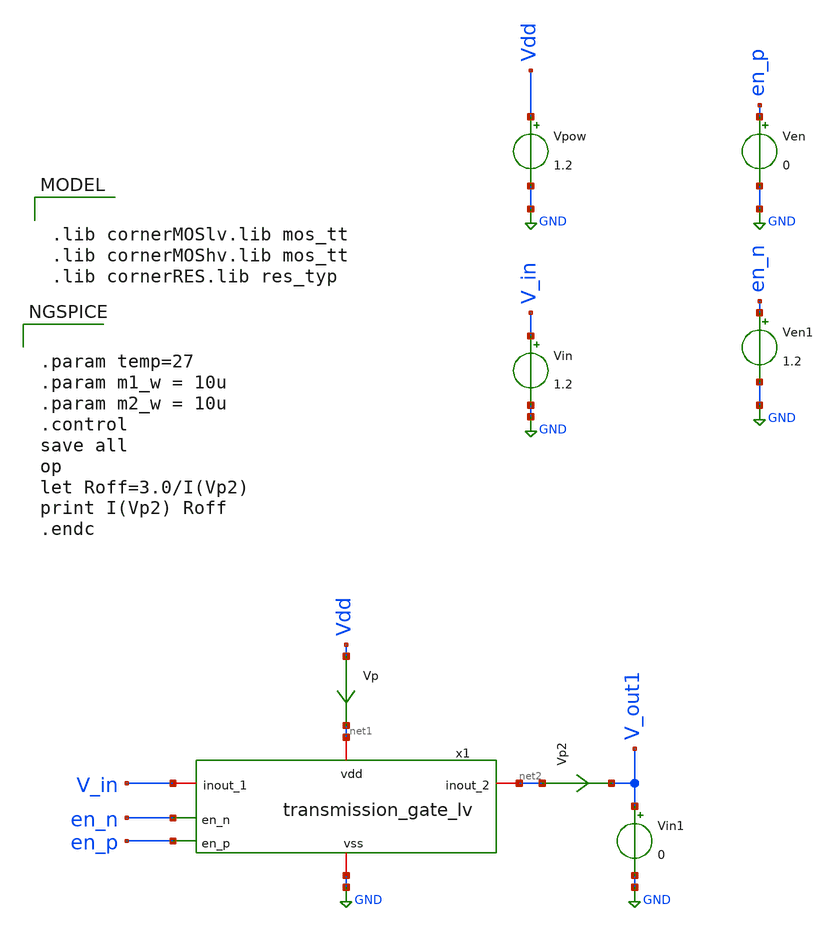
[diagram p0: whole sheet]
** sch_path: design_data/xschem/transmission_gate__lv_tb_Ileak.sch
* Copyright 2023 IHP PDK Authors
**.subckt transmission_gate__lv_tb_Ileak
Vpow Vdd GND 1.2
Vp Vdd net1 0
.save i(vp)
Vin V_in GND 1.2
Ven en_p GND 0
Ven1 en_n GND 1.2
Vp2 net2 V_out1 0
.save i(vp2)
Vin1 V_out1 GND 0
x1 net1 en_n V_in net2 en_p GND transmission_gate_lv
**** begin user architecture code

.lib cornerMOSlv.lib mos_tt
.lib cornerMOShv.lib mos_tt
.lib cornerRES.lib res_typ



.param temp=27
.param m1_w = 10u
.param m2_w = 10u
.control
save all
op
let Roff=3.0/I(Vp2)
print I(Vp2) Roff
.endc


**** end user architecture code
**.ends

* expanding   symbol:  transmission_gate_lv.sym # of pins=6
** sym_path: design_data/xschem/transmission_gate_lv.sym
** sch_path: design_data/xschem/transmission_gate_lv.sch
.subckt transmission_gate_lv vdd en_n inout_1 inout_2 en_p vss
*.iopin inout_1
*.iopin inout_2
*.ipin en_p
*.iopin vdd
*.iopin vss
*.ipin en_n
XR1 vss net1 ptap1 R=1.903 w=20.78e-6 l=20.78e-6
XR2 vdd net2 ntap1 R=1.903 w=20.78e-6 l=20.78e-6
XM2 inout_2 en_n inout_1 net2 sg13_lv_pmos w={m2_w} l=0.13u ng=10 m=1 mm_ok=1
XM1 inout_1 en_p inout_2 net1 sg13_lv_nmos w={m1_w} l=0.13u ng=10 m=1 mm_ok=1
.ends

.GLOBAL GND
.end
